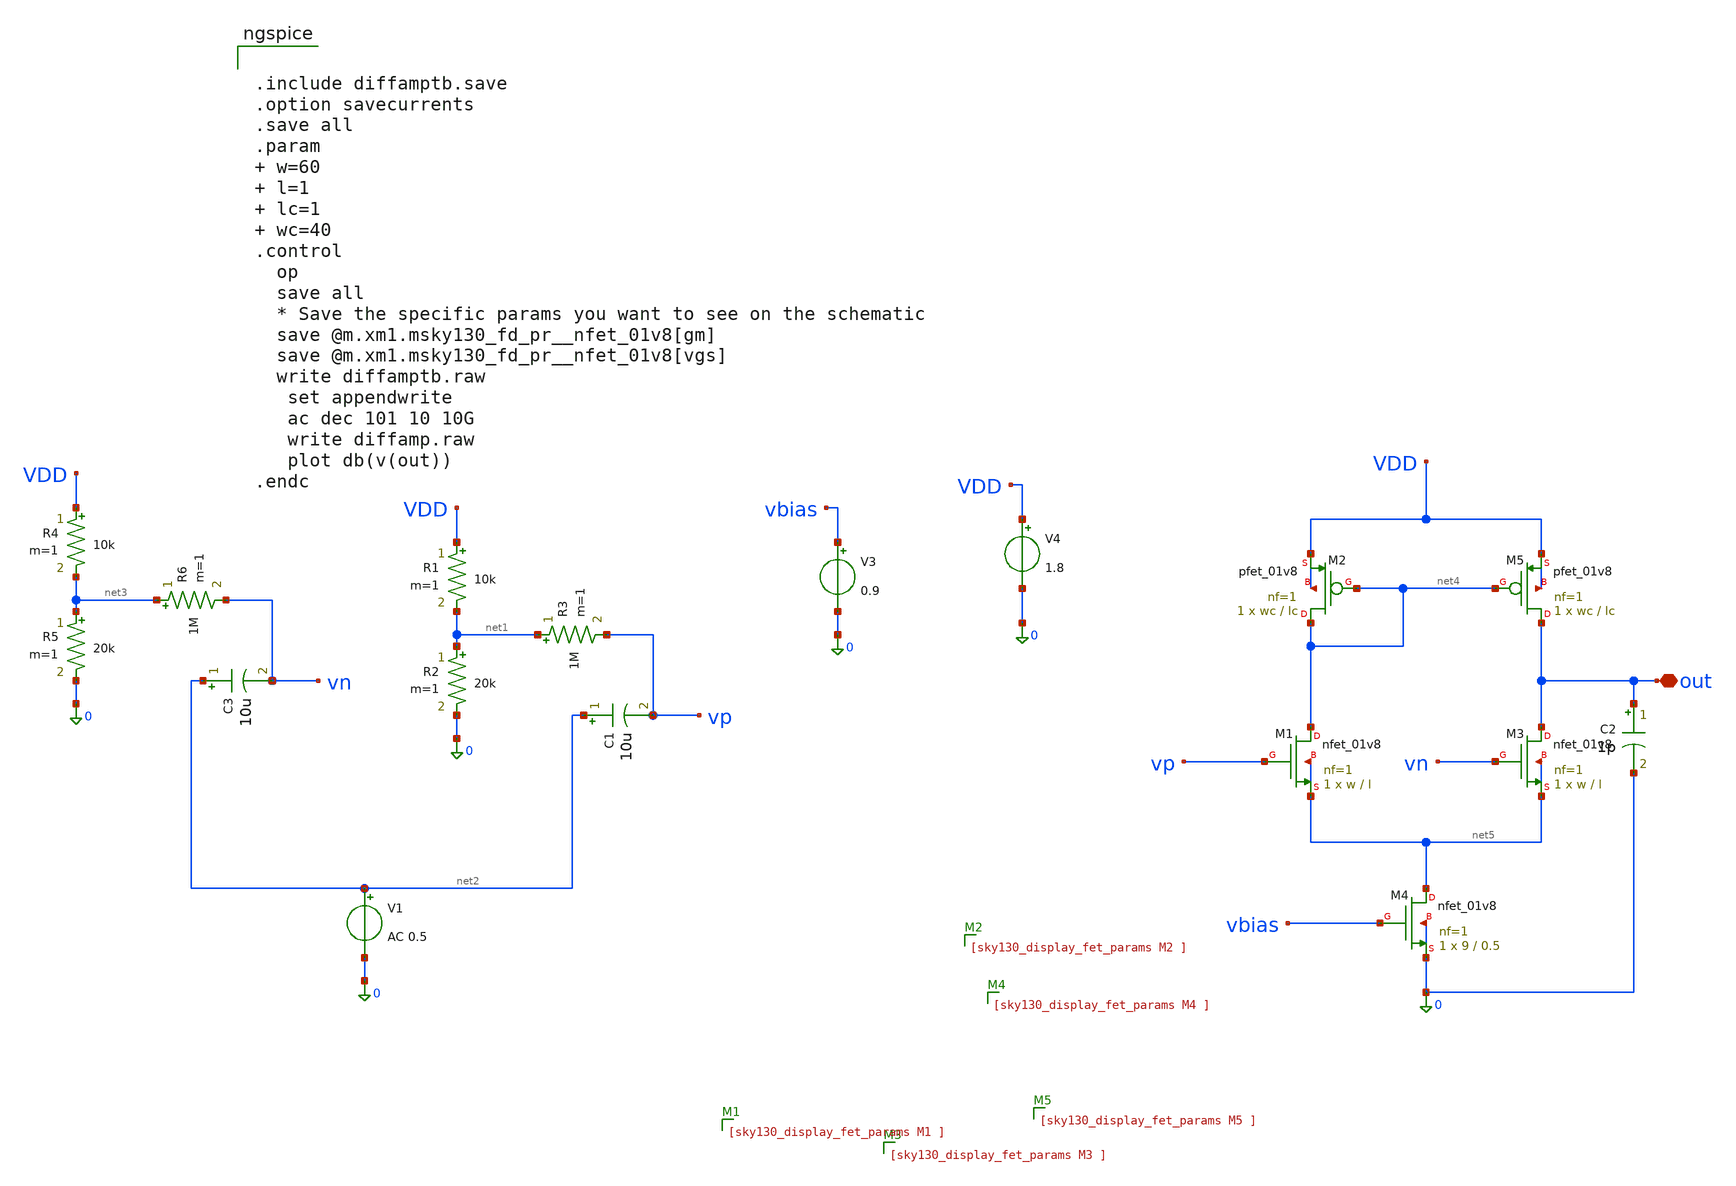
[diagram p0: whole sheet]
** sch_path: design_data/xschem/diffamptb.sch
**.subckt diffamptb out
*.iopin out
V1 net2 0 AC 0.5
R1 VDD net1 10k m=1
R2 net1 0 20k m=1
R3 net1 vp 1M m=1
C1 net2 vp 10u m=1
R4 VDD net3 10k m=1
R5 net3 0 20k m=1
R6 net3 vn 1M m=1
C3 net2 vn 10u m=1
V3 vbias 0 0.9
V4 VDD 0 1.8
XM2 net4 net4 VDD VDD sky130_fd_pr__pfet_01v8 L=lc W=wc nf=1 ad='int((1 + 1)/2) * wc / 1 * 0.29' as='int((1 + 2)/2) * wc / 1 * 0.29'
+ pd='2*int((1 + 1)/2) * (wc / 1 + 0.29)' ps='2*int((1 + 2)/2) * (wc / 1 + 0.29)' nrd='0.29 / wc ' nrs='0.29 / wc '
+ sa=0 sb=0 sd=0 mult=1 m=1
XM3 out vn net5 net5 sky130_fd_pr__nfet_01v8 L=l W=w nf=1 ad='int((1 + 1)/2) * w / 1 * 0.29' as='int((1 + 2)/2) * w / 1 * 0.29'
+ pd='2*int((1 + 1)/2) * (w / 1 + 0.29)' ps='2*int((1 + 2)/2) * (w / 1 + 0.29)' nrd='0.29 / w ' nrs='0.29 / w '
+ sa=0 sb=0 sd=0 mult=1 m=1
XM1 net4 vp net5 net5 sky130_fd_pr__nfet_01v8 L=l W=w nf=1 ad='int((1 + 1)/2) * w / 1 * 0.29' as='int((1 + 2)/2) * w / 1 * 0.29'
+ pd='2*int((1 + 1)/2) * (w / 1 + 0.29)' ps='2*int((1 + 2)/2) * (w / 1 + 0.29)' nrd='0.29 / w ' nrs='0.29 / w '
+ sa=0 sb=0 sd=0 mult=1 m=1
XM4 net5 vbias 0 0 sky130_fd_pr__nfet_01v8 L=0.5 W=9 nf=1 ad='int((1 + 1)/2) * 9 / 1 * 0.29' as='int((1 + 2)/2) * 9 / 1 * 0.29'
+ pd='2*int((1 + 1)/2) * (9 / 1 + 0.29)' ps='2*int((1 + 2)/2) * (9 / 1 + 0.29)' nrd='0.29 / 9 ' nrs='0.29 / 9 '
+ sa=0 sb=0 sd=0 mult=1 m=1
XM5 out net4 VDD VDD sky130_fd_pr__pfet_01v8 L=lc W=wc nf=1 ad='int((1 + 1)/2) * wc / 1 * 0.29' as='int((1 + 2)/2) * wc / 1 * 0.29'
+ pd='2*int((1 + 1)/2) * (wc / 1 + 0.29)' ps='2*int((1 + 2)/2) * (wc / 1 + 0.29)' nrd='0.29 / wc ' nrs='0.29 / wc '
+ sa=0 sb=0 sd=0 mult=1 m=1
C2 out 0 1p m=1
**** begin user architecture code


.include diffamptb.save
.option savecurrents
.save all
.param  w=60  l=1  lc=1  wc=40
.control
  op
  save all
  * Save the specific params you want to see on the schematic
  save @m.xm1.msky130_fd_pr__nfet_01v8[gm]
  save @m.xm1.msky130_fd_pr__nfet_01v8[vgs]
  write diffamptb.raw
   set appendwrite
   ac dec 101 10 10G
   write diffamp.raw
   plot db(v(out))
.endc



** opencircuitdesign pdks install
.lib $::SKYWATER_MODELS/sky130.lib.spice tt

**** end user architecture code
**.ends
.end
